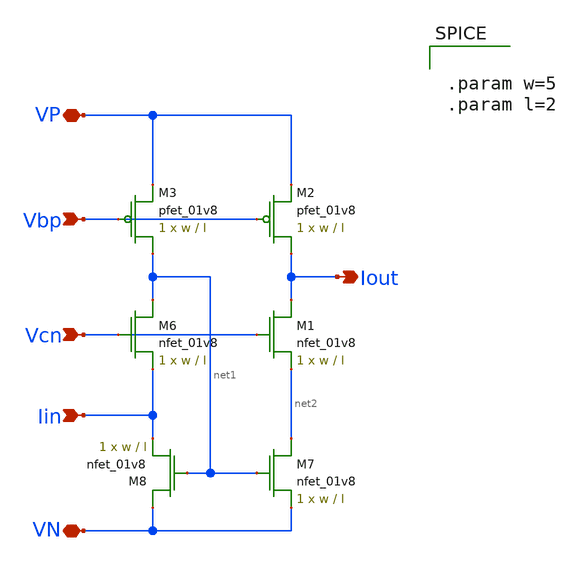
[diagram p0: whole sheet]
** sch_path: schematic/iout_mirror.sch
**.subckt iout_mirror Vbp VN Iout Iin Vcn VP
*.ipin Vbp
*.iopin VN
*.opin Iout
*.ipin Iin
*.ipin Vcn
*.iopin VP
XM1 Iout Vcn net2 GND sky130_fd_pr__nfet_01v8 L=l W=w nf=1 ad='int((nf+1)/2) * W/nf * 0.29' as='int((nf+2)/2) * W/nf * 0.29'
+ pd='2*int((nf+1)/2) * (W/nf + 0.29)' ps='2*int((nf+2)/2) * (W/nf + 0.29)' nrd='0.29 / W' nrs='0.29 / W'
+ sa=0 sb=0 sd=0 mult=1 m=1
XM2 Iout Vbp VP VDD sky130_fd_pr__pfet_01v8 L=l W=w nf=1 ad='int((nf+1)/2) * W/nf * 0.29' as='int((nf+2)/2) * W/nf * 0.29'
+ pd='2*int((nf+1)/2) * (W/nf + 0.29)' ps='2*int((nf+2)/2) * (W/nf + 0.29)' nrd='0.29 / W' nrs='0.29 / W'
+ sa=0 sb=0 sd=0 mult=1 m=1
XM3 net1 Vbp VP VDD sky130_fd_pr__pfet_01v8 L=l W=w nf=1 ad='int((nf+1)/2) * W/nf * 0.29' as='int((nf+2)/2) * W/nf * 0.29'
+ pd='2*int((nf+1)/2) * (W/nf + 0.29)' ps='2*int((nf+2)/2) * (W/nf + 0.29)' nrd='0.29 / W' nrs='0.29 / W'
+ sa=0 sb=0 sd=0 mult=1 m=1
XM6 net1 Vcn Iin GND sky130_fd_pr__nfet_01v8 L=l W=w nf=1 ad='int((nf+1)/2) * W/nf * 0.29' as='int((nf+2)/2) * W/nf * 0.29'
+ pd='2*int((nf+1)/2) * (W/nf + 0.29)' ps='2*int((nf+2)/2) * (W/nf + 0.29)' nrd='0.29 / W' nrs='0.29 / W'
+ sa=0 sb=0 sd=0 mult=1 m=1
XM7 net2 net1 VN GND sky130_fd_pr__nfet_01v8 L=l W=w nf=1 ad='int((nf+1)/2) * W/nf * 0.29' as='int((nf+2)/2) * W/nf * 0.29'
+ pd='2*int((nf+1)/2) * (W/nf + 0.29)' ps='2*int((nf+2)/2) * (W/nf + 0.29)' nrd='0.29 / W' nrs='0.29 / W'
+ sa=0 sb=0 sd=0 mult=1 m=1
XM8 VN net1 Iin GND sky130_fd_pr__nfet_01v8 L=l W=w nf=1 ad='int((nf+1)/2) * W/nf * 0.29' as='int((nf+2)/2) * W/nf * 0.29'
+ pd='2*int((nf+1)/2) * (W/nf + 0.29)' ps='2*int((nf+2)/2) * (W/nf + 0.29)' nrd='0.29 / W' nrs='0.29 / W'
+ sa=0 sb=0 sd=0 mult=1 m=1
**** begin user architecture code


.param w=5
.param l=2


**** end user architecture code
**.ends
.end
